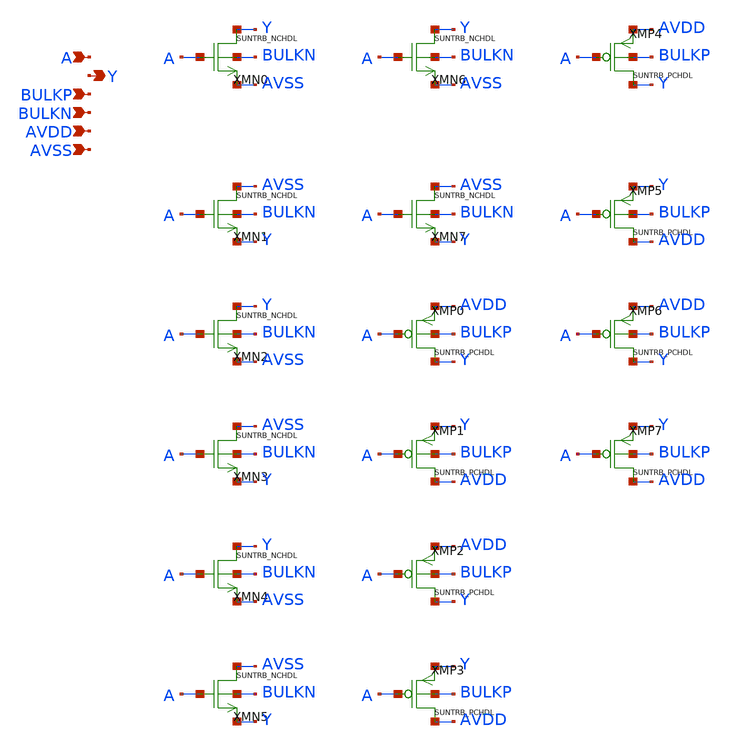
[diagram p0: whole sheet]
** sch_path: design/SUN_TRB_SKY130NM/SUNTRB_IVX8_CV.sch
**.subckt SUNTRB_IVX8_CV A Y BULKP BULKN AVDD AVSS
*.ipin A
*.opin Y
*.ipin BULKP
*.ipin BULKN
*.ipin AVDD
*.ipin AVSS
XMN0 Y A AVSS BULKN SUNTRB_NCHDL xoffset=0 yoffset=0 angle=0
XMN1 AVSS A Y BULKN SUNTRB_NCHDL xoffset=0 yoffset=0 angle=0
XMN2 Y A AVSS BULKN SUNTRB_NCHDL xoffset=0 yoffset=0 angle=0
XMN3 AVSS A Y BULKN SUNTRB_NCHDL xoffset=0 yoffset=0 angle=0
XMN4 Y A AVSS BULKN SUNTRB_NCHDL xoffset=0 yoffset=0 angle=0
XMN5 AVSS A Y BULKN SUNTRB_NCHDL xoffset=0 yoffset=0 angle=0
XMN6 Y A AVSS BULKN SUNTRB_NCHDL xoffset=0 yoffset=0 angle=0
XMN7 AVSS A Y BULKN SUNTRB_NCHDL xoffset=0 yoffset=0 angle=0
XMP0 Y A AVDD BULKP SUNTRB_PCHDL xoffset=0 yoffset=0 angle=0 M=1
XMP1 AVDD A Y BULKP SUNTRB_PCHDL xoffset=0 yoffset=0 angle=0 M=1
XMP2 Y A AVDD BULKP SUNTRB_PCHDL xoffset=0 yoffset=0 angle=0 M=1
XMP3 AVDD A Y BULKP SUNTRB_PCHDL xoffset=0 yoffset=0 angle=0 M=1
XMP4 Y A AVDD BULKP SUNTRB_PCHDL xoffset=0 yoffset=0 angle=0 M=1
XMP5 AVDD A Y BULKP SUNTRB_PCHDL xoffset=0 yoffset=0 angle=0 M=1
XMP6 Y A AVDD BULKP SUNTRB_PCHDL xoffset=0 yoffset=0 angle=0 M=1
XMP7 AVDD A Y BULKP SUNTRB_PCHDL xoffset=0 yoffset=0 angle=0 M=1
**.ends
.end
